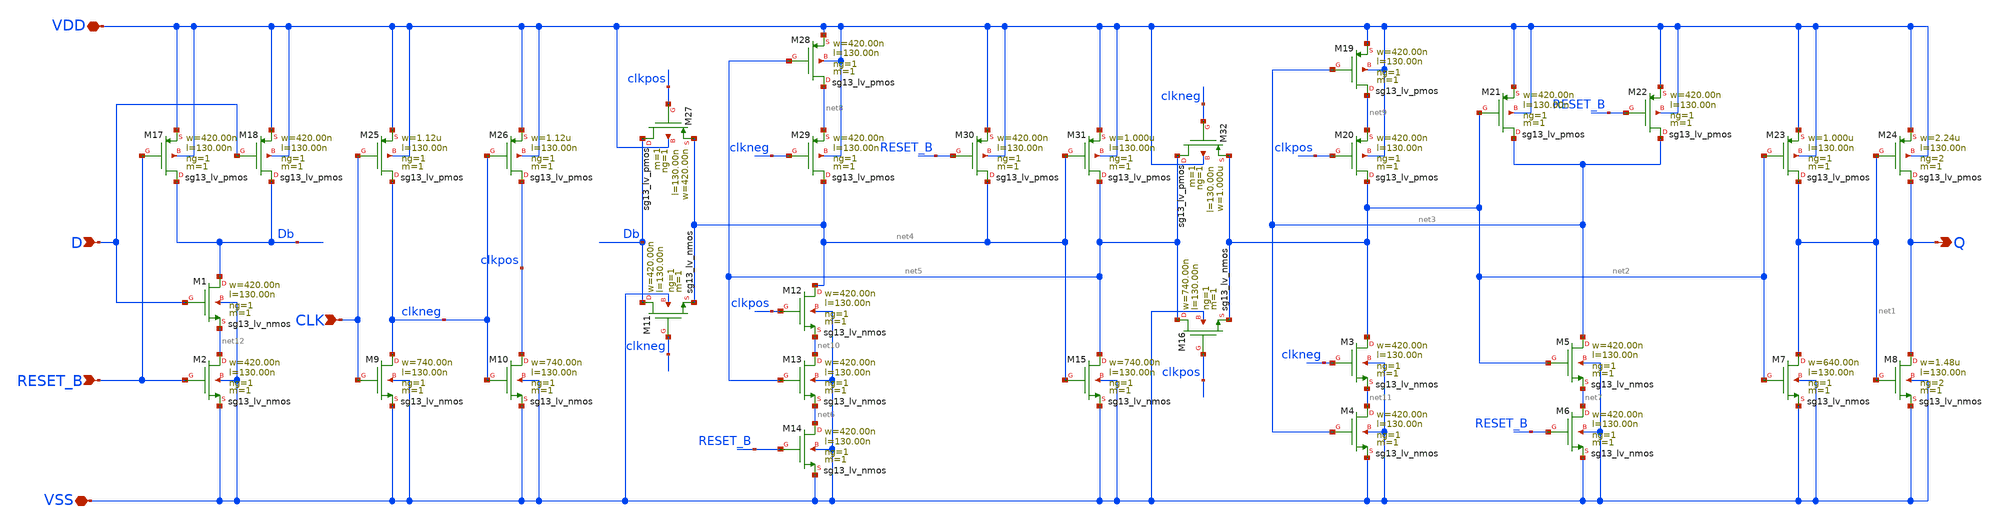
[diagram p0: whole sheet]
** sch_path: ihp-sg13g2/libs.tech/xschem/sg13g2_stdcells/sg13g2_dfrbpq_2.sch
**.subckt sg13g2_dfrbpq_2 Q CLK D RESET_B VDD VSS
*.opin Q
*.ipin CLK
*.ipin D
*.ipin RESET_B
*.iopin VDD
*.iopin VSS
XM1 Db D net12 VSS sg13_lv_nmos w=420.00n l=130.00n ng=1 m=1 mm_ok=1
XM2 net12 RESET_B VSS VSS sg13_lv_nmos w=420.00n l=130.00n ng=1 m=1 mm_ok=1
XM3 net2 clkneg net11 VSS sg13_lv_nmos w=420.00n l=130.00n ng=1 m=1 mm_ok=1
XM4 net11 net3 VSS VSS sg13_lv_nmos w=420.00n l=130.00n ng=1 m=1 mm_ok=1
XM5 net3 net2 net7 VSS sg13_lv_nmos w=420.00n l=130.00n ng=1 m=1 mm_ok=1
XM6 net7 RESET_B VSS VSS sg13_lv_nmos w=420.00n l=130.00n ng=1 m=1 mm_ok=1
XM7 net1 net2 VSS VSS sg13_lv_nmos w=640.00n l=130.00n ng=1 m=1 mm_ok=1
XM8 Q net1 VSS VSS sg13_lv_nmos w=1.48u l=130.00n ng=2 m=1 mm_ok=1
XM9 clkneg CLK VSS VSS sg13_lv_nmos w=740.00n l=130.00n ng=1 m=1 mm_ok=1
XM10 clkpos clkneg VSS VSS sg13_lv_nmos w=740.00n l=130.00n ng=1 m=1 mm_ok=1
XM11 Db clkneg net4 VSS sg13_lv_nmos w=420.00n l=130.00n ng=1 m=1 mm_ok=1
XM12 net4 clkpos net10 VSS sg13_lv_nmos w=420.00n l=130.00n ng=1 m=1 mm_ok=1
XM13 net10 net5 net6 VSS sg13_lv_nmos w=420.00n l=130.00n ng=1 m=1 mm_ok=1
XM14 net6 RESET_B VSS VSS sg13_lv_nmos w=420.00n l=130.00n ng=1 m=1 mm_ok=1
XM15 net5 net4 VSS VSS sg13_lv_nmos w=740.00n l=130.00n ng=1 m=1 mm_ok=1
XM16 net5 clkpos net2 VSS sg13_lv_nmos w=740.00n l=130.00n ng=1 m=1 mm_ok=1
XM17 Db RESET_B VDD VDD sg13_lv_pmos w=420.00n l=130.00n ng=1 m=1 mm_ok=1
XM18 Db D VDD VDD sg13_lv_pmos w=420.00n l=130.00n ng=1 m=1 mm_ok=1
XM19 net9 net3 VDD VDD sg13_lv_pmos w=420.00n l=130.00n ng=1 m=1 mm_ok=1
XM20 net2 clkpos net9 VDD sg13_lv_pmos w=420.00n l=130.00n ng=1 m=1 mm_ok=1
XM21 net3 net2 VDD VDD sg13_lv_pmos w=420.00n l=130.00n ng=1 m=1 mm_ok=1
XM22 net3 RESET_B VDD VDD sg13_lv_pmos w=420.00n l=130.00n ng=1 m=1 mm_ok=1
XM23 net1 net2 VDD VDD sg13_lv_pmos w=1.000u l=130.00n ng=1 m=1 mm_ok=1
XM24 Q net1 VDD VDD sg13_lv_pmos w=2.24u l=130.00n ng=2 m=1 mm_ok=1
XM25 clkneg CLK VDD VDD sg13_lv_pmos w=1.12u l=130.00n ng=1 m=1 mm_ok=1
XM26 clkpos clkneg VDD VDD sg13_lv_pmos w=1.12u l=130.00n ng=1 m=1 mm_ok=1
XM27 Db clkpos net4 VDD sg13_lv_pmos w=420.00n l=130.00n ng=1 m=1 mm_ok=1
XM28 net8 net5 VDD VDD sg13_lv_pmos w=420.00n l=130.00n ng=1 m=1 mm_ok=1
XM29 net4 clkneg net8 VDD sg13_lv_pmos w=420.00n l=130.00n ng=1 m=1 mm_ok=1
XM30 net4 RESET_B VDD VDD sg13_lv_pmos w=420.00n l=130.00n ng=1 m=1 mm_ok=1
XM31 net5 net4 VDD VDD sg13_lv_pmos w=1.000u l=130.00n ng=1 m=1 mm_ok=1
XM32 net5 clkneg net2 VDD sg13_lv_pmos w=1.000u l=130.00n ng=1 m=1 mm_ok=1
**.ends
.end
